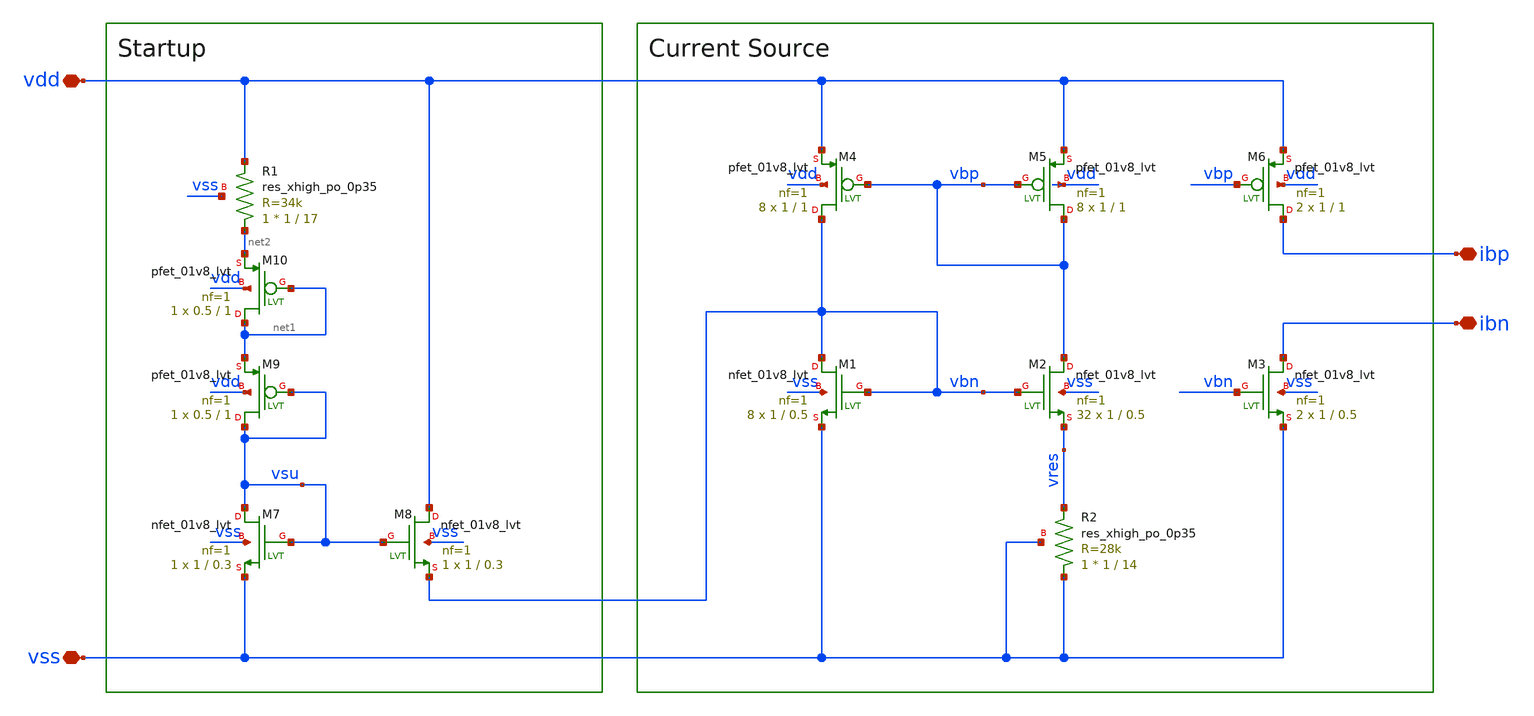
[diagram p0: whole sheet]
** sch_path: xschem/bias/bias_basis_current.sch
**.subckt bias_basis_current ibn vdd vss ibp
*.iopin ibn
*.iopin vdd
*.iopin vss
*.iopin ibp
XM5 vbp vbp vdd vdd sky130_fd_pr__pfet_01v8_lvt L=1 W=1 nf=1 ad='int((nf+1)/2) * W/nf * 0.29' as='int((nf+2)/2) * W/nf * 0.29'
+ pd='2*int((nf+1)/2) * (W/nf + 0.29)' ps='2*int((nf+2)/2) * (W/nf + 0.29)' nrd='0.29 / W' nrs='0.29 / W'
+ sa=0 sb=0 sd=0 mult=8 m=8
XM4 vbn vbp vdd vdd sky130_fd_pr__pfet_01v8_lvt L=1 W=1 nf=1 ad='int((nf+1)/2) * W/nf * 0.29' as='int((nf+2)/2) * W/nf * 0.29'
+ pd='2*int((nf+1)/2) * (W/nf + 0.29)' ps='2*int((nf+2)/2) * (W/nf + 0.29)' nrd='0.29 / W' nrs='0.29 / W'
+ sa=0 sb=0 sd=0 mult=8 m=8
XM1 vbn vbn vss vss sky130_fd_pr__nfet_01v8_lvt L=0.5 W=1 nf=1 ad='int((nf+1)/2) * W/nf * 0.29' as='int((nf+2)/2) * W/nf * 0.29'
+ pd='2*int((nf+1)/2) * (W/nf + 0.29)' ps='2*int((nf+2)/2) * (W/nf + 0.29)' nrd='0.29 / W' nrs='0.29 / W'
+ sa=0 sb=0 sd=0 mult=8 m=8
XM2 vbp vbn vres vss sky130_fd_pr__nfet_01v8_lvt L=0.5 W=1 nf=1 ad='int((nf+1)/2) * W/nf * 0.29' as='int((nf+2)/2) * W/nf * 0.29'
+ pd='2*int((nf+1)/2) * (W/nf + 0.29)' ps='2*int((nf+2)/2) * (W/nf + 0.29)' nrd='0.29 / W' nrs='0.29 / W'
+ sa=0 sb=0 sd=0 mult=32 m=32
XM6 ibp vbp vdd vdd sky130_fd_pr__pfet_01v8_lvt L=1 W=1 nf=1 ad='int((nf+1)/2) * W/nf * 0.29' as='int((nf+2)/2) * W/nf * 0.29'
+ pd='2*int((nf+1)/2) * (W/nf + 0.29)' ps='2*int((nf+2)/2) * (W/nf + 0.29)' nrd='0.29 / W' nrs='0.29 / W'
+ sa=0 sb=0 sd=0 mult=2 m=2
XM3 ibn vbn vss vss sky130_fd_pr__nfet_01v8_lvt L=0.5 W=1 nf=1 ad='int((nf+1)/2) * W/nf * 0.29' as='int((nf+2)/2) * W/nf * 0.29'
+ pd='2*int((nf+1)/2) * (W/nf + 0.29)' ps='2*int((nf+2)/2) * (W/nf + 0.29)' nrd='0.29 / W' nrs='0.29 / W'
+ sa=0 sb=0 sd=0 mult=2 m=2
XM7 vsu vsu vss vss sky130_fd_pr__nfet_01v8_lvt L=0.3 W=1 nf=1 ad='int((nf+1)/2) * W/nf * 0.29' as='int((nf+2)/2) * W/nf * 0.29'
+ pd='2*int((nf+1)/2) * (W/nf + 0.29)' ps='2*int((nf+2)/2) * (W/nf + 0.29)' nrd='0.29 / W' nrs='0.29 / W'
+ sa=0 sb=0 sd=0 mult=1 m=1
XM8 vdd vsu vbn vss sky130_fd_pr__nfet_01v8_lvt L=0.3 W=1 nf=1 ad='int((nf+1)/2) * W/nf * 0.29' as='int((nf+2)/2) * W/nf * 0.29'
+ pd='2*int((nf+1)/2) * (W/nf + 0.29)' ps='2*int((nf+2)/2) * (W/nf + 0.29)' nrd='0.29 / W' nrs='0.29 / W'
+ sa=0 sb=0 sd=0 mult=1 m=1
XM9 vsu vsu net1 vdd sky130_fd_pr__pfet_01v8_lvt L=1 W=0.5 nf=1 ad='int((nf+1)/2) * W/nf * 0.29' as='int((nf+2)/2) * W/nf * 0.29'
+ pd='2*int((nf+1)/2) * (W/nf + 0.29)' ps='2*int((nf+2)/2) * (W/nf + 0.29)' nrd='0.29 / W' nrs='0.29 / W'
+ sa=0 sb=0 sd=0 mult=1 m=1
XM10 net1 net1 net2 vdd sky130_fd_pr__pfet_01v8_lvt L=1 W=0.5 nf=1 ad='int((nf+1)/2) * W/nf * 0.29' as='int((nf+2)/2) * W/nf * 0.29'
+ pd='2*int((nf+1)/2) * (W/nf + 0.29)' ps='2*int((nf+2)/2) * (W/nf + 0.29)' nrd='0.29 / W' nrs='0.29 / W'
+ sa=0 sb=0 sd=0 mult=1 m=1
XR2 vss vres vss sky130_fd_pr__res_xhigh_po_0p35 W=1 L=14 mult=1 m=1
XR1 net2 vdd vss sky130_fd_pr__res_xhigh_po_0p35 W=1 L=17 mult=1 m=1
**.ends
.end
